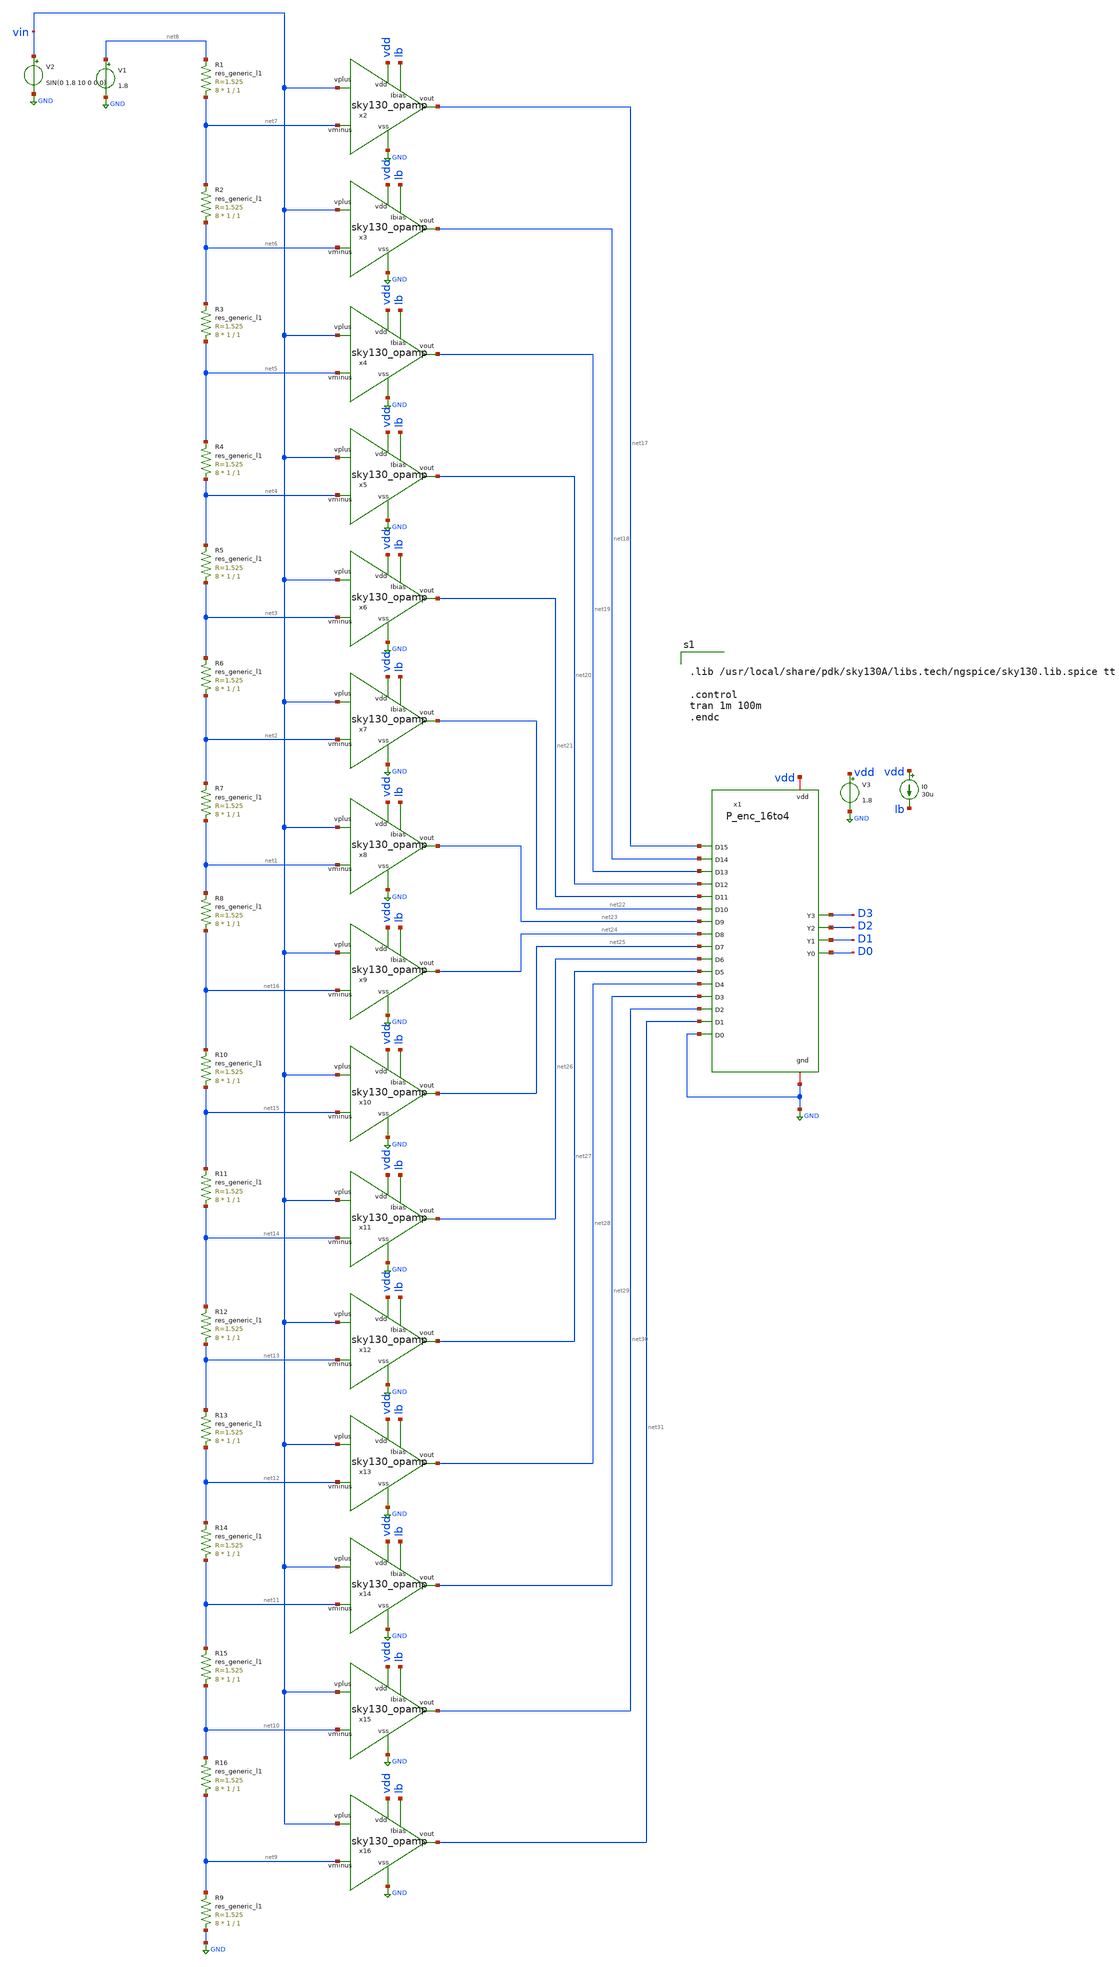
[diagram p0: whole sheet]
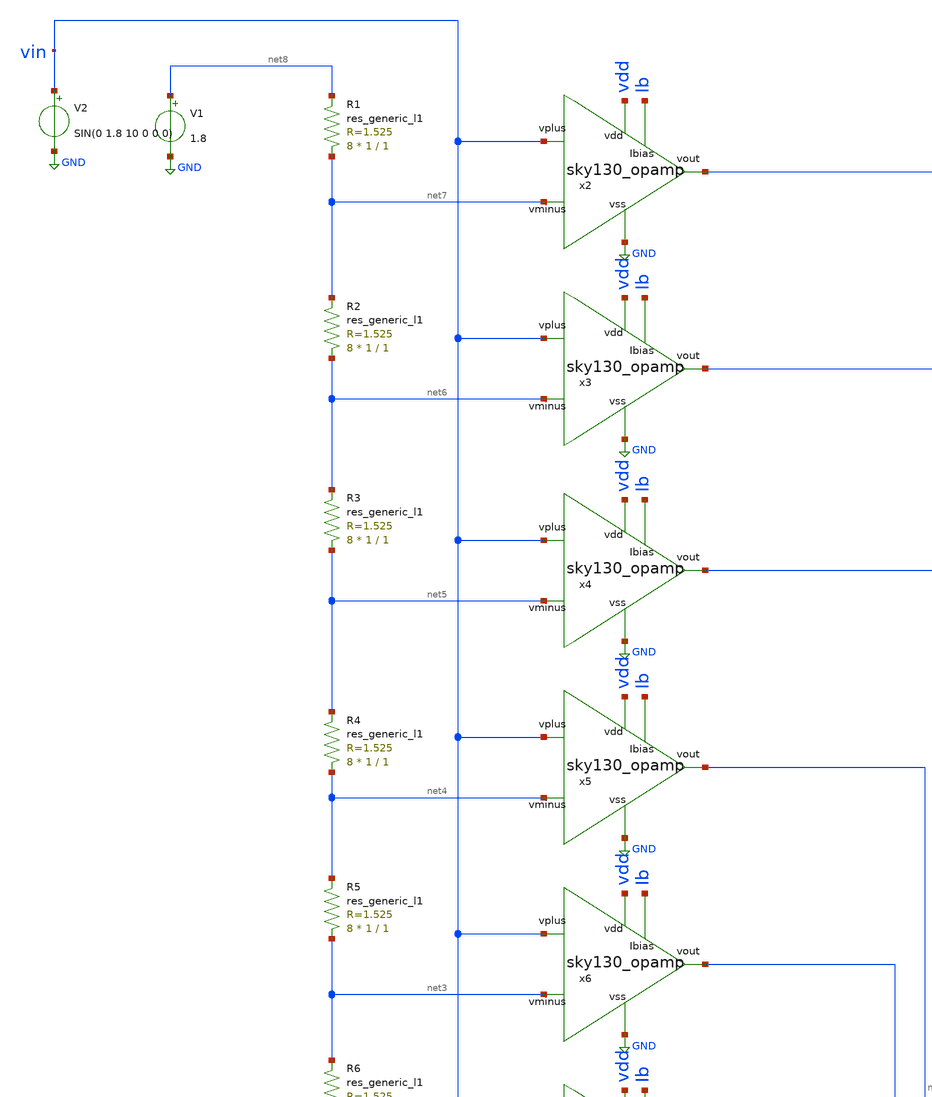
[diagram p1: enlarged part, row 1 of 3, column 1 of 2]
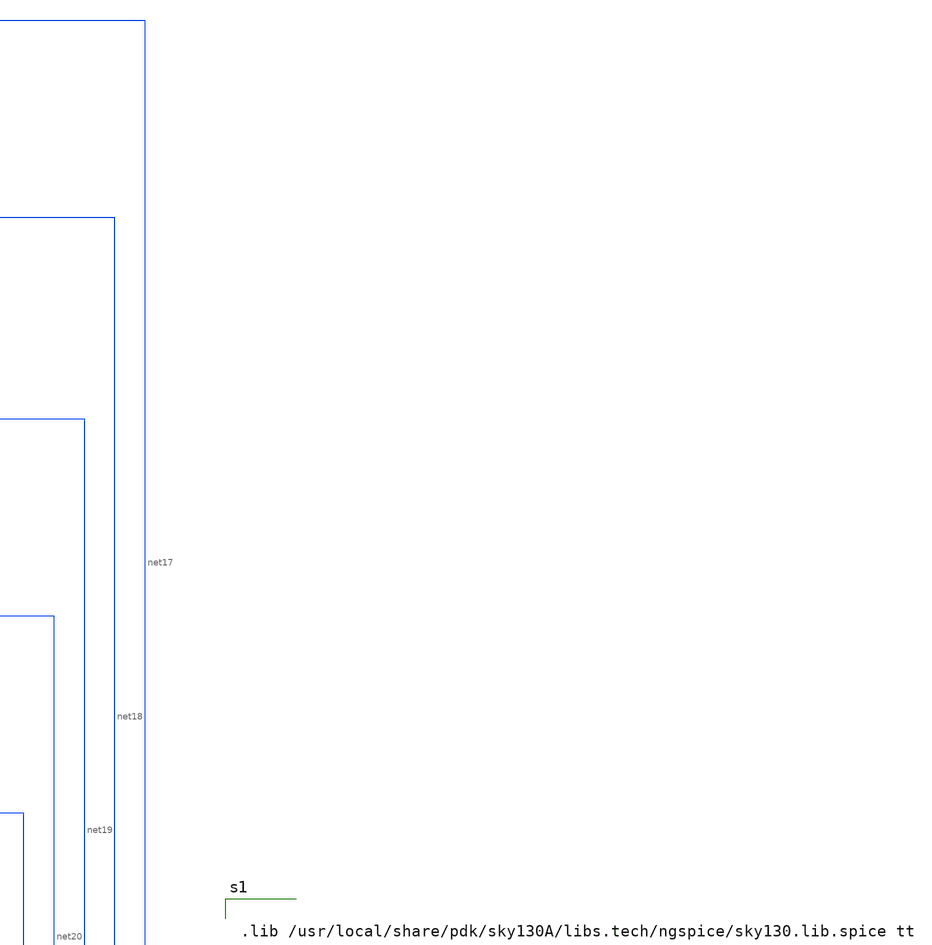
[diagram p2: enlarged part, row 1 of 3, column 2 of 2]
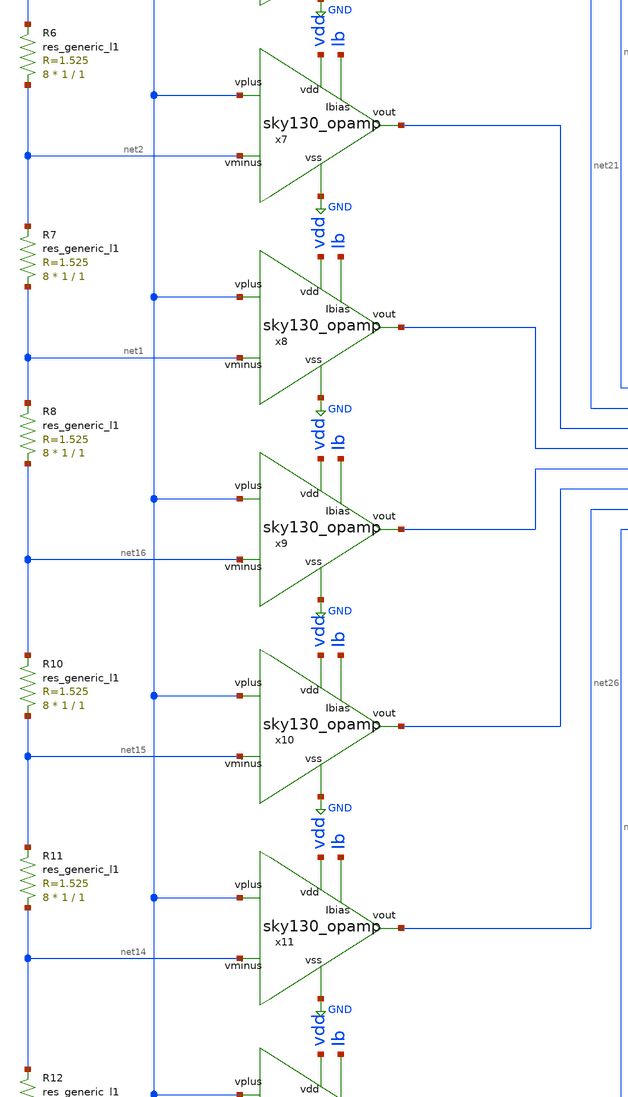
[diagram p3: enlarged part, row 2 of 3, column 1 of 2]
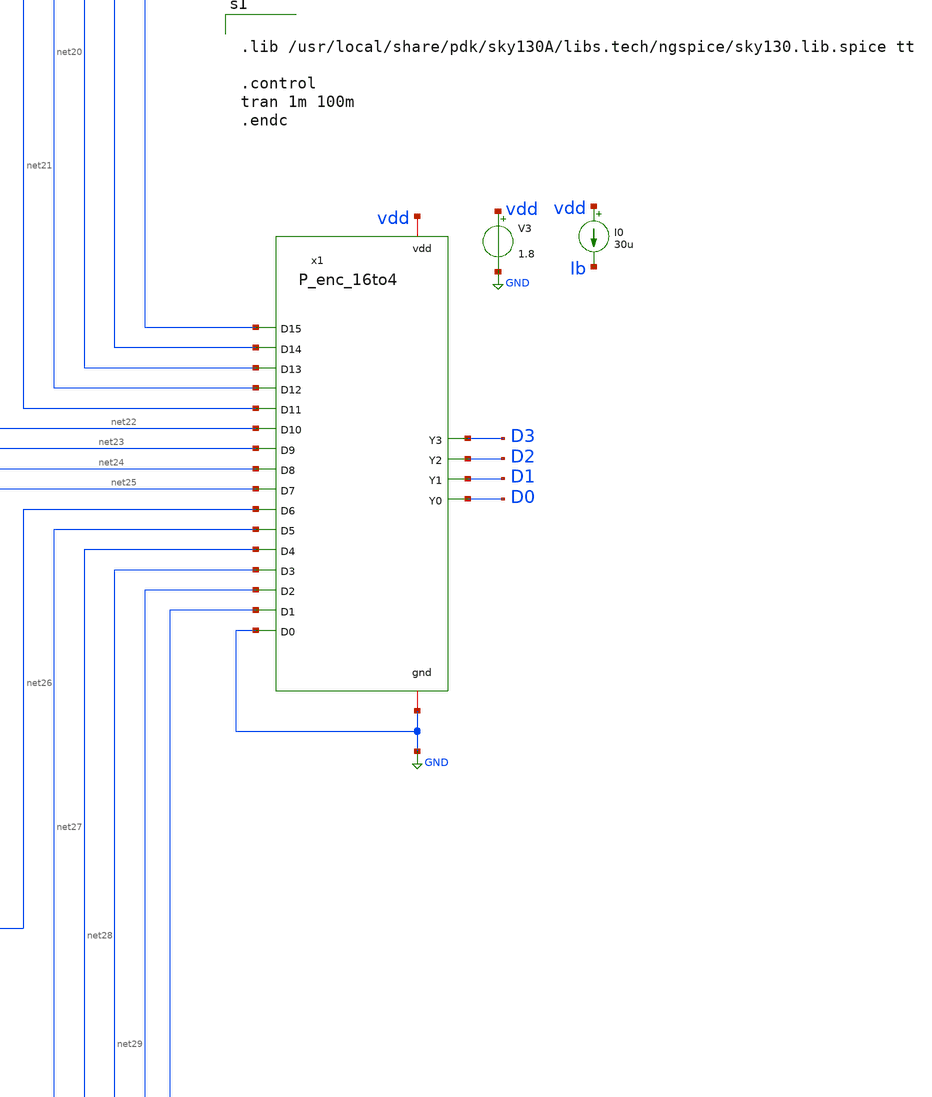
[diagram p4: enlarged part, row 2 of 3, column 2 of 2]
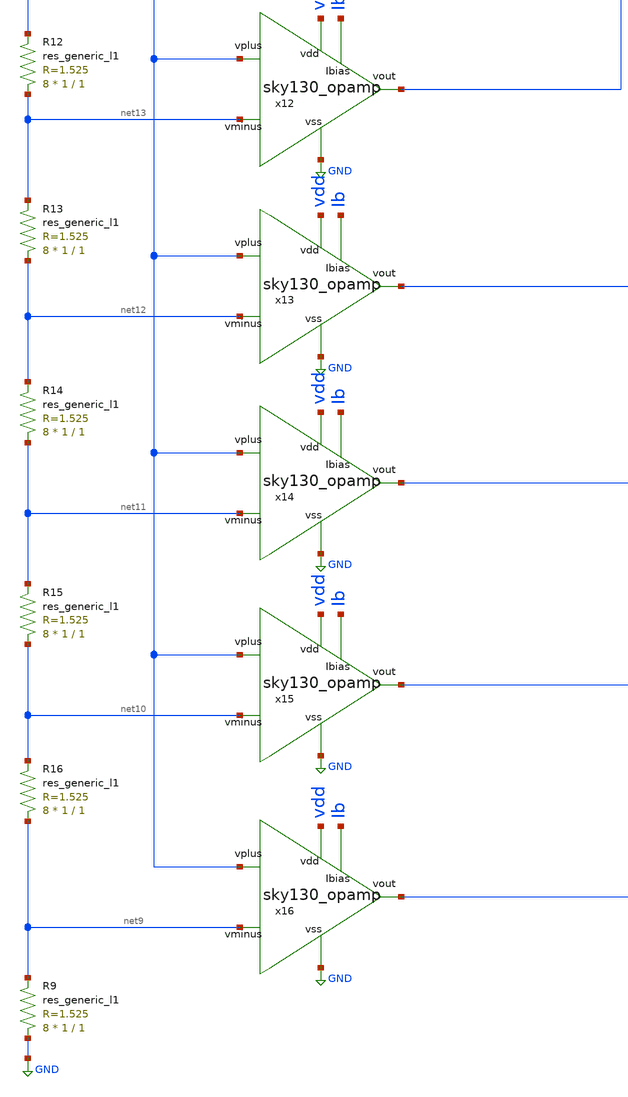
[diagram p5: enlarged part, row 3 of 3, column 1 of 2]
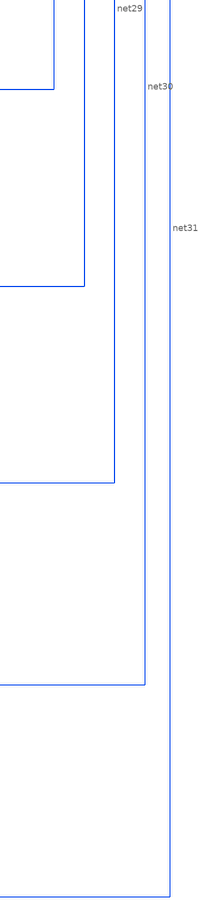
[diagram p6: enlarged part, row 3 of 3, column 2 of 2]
** sch_path: Analog to Digital Converter (Flash ADC)/Flash_adc_4bit.sch
**.subckt Flash_adc_4bit
x1 D3 vdd GND net17 net18 net19 D2 net20 net21 net22 D1 net23 net24 net25 net26 D0 net27 net28 net29
+ net30 net31 GND P_enc_16to4
x2 vdd net17 vin net7 Ib GND sky130_opamp
R1 net7 net8 sky130_fd_pr__res_generic_l1 W=1 L=1 m=8
R2 net6 net7 sky130_fd_pr__res_generic_l1 W=1 L=1 m=8
R3 net5 net6 sky130_fd_pr__res_generic_l1 W=1 L=1 m=8
R4 net4 net5 sky130_fd_pr__res_generic_l1 W=1 L=1 m=8
R5 net3 net4 sky130_fd_pr__res_generic_l1 W=1 L=1 m=8
R6 net2 net3 sky130_fd_pr__res_generic_l1 W=1 L=1 m=8
R7 net1 net2 sky130_fd_pr__res_generic_l1 W=1 L=1 m=8
R8 net16 net1 sky130_fd_pr__res_generic_l1 W=1 L=1 m=8
x3 vdd net18 vin net6 Ib GND sky130_opamp
x4 vdd net19 vin net5 Ib GND sky130_opamp
x5 vdd net20 vin net4 Ib GND sky130_opamp
x6 vdd net21 vin net3 Ib GND sky130_opamp
x7 vdd net22 vin net2 Ib GND sky130_opamp
x8 vdd net23 vin net1 Ib GND sky130_opamp
x9 vdd net24 vin net16 Ib GND sky130_opamp
x10 vdd net25 vin net15 Ib GND sky130_opamp
x11 vdd net26 vin net14 Ib GND sky130_opamp
x12 vdd net27 vin net13 Ib GND sky130_opamp
x13 vdd net28 vin net12 Ib GND sky130_opamp
x14 vdd net29 vin net11 Ib GND sky130_opamp
x15 vdd net30 vin net10 Ib GND sky130_opamp
R10 net15 net16 sky130_fd_pr__res_generic_l1 W=1 L=1 m=8
R11 net14 net15 sky130_fd_pr__res_generic_l1 W=1 L=1 m=8
R12 net13 net14 sky130_fd_pr__res_generic_l1 W=1 L=1 m=8
R13 net12 net13 sky130_fd_pr__res_generic_l1 W=1 L=1 m=8
R14 net11 net12 sky130_fd_pr__res_generic_l1 W=1 L=1 m=8
R15 net10 net11 sky130_fd_pr__res_generic_l1 W=1 L=1 m=8
R16 net9 net10 sky130_fd_pr__res_generic_l1 W=1 L=1 m=8
x16 vdd net31 vin net9 Ib GND sky130_opamp
R9 GND net9 sky130_fd_pr__res_generic_l1 W=1 L=1 m=8
V1 net8 GND 1.8
V2 vin GND SIN(0 1.8 10 0 0 0)
V3 vdd GND 1.8
I0 vdd Ib 30u
**** begin user architecture code


.lib /usr/local/share/pdk/sky130A/libs.tech/ngspice/sky130.lib.spice tt

.control
tran 1m 100m
.endc


**** end user architecture code
**.ends

* expanding   symbol:  /home/rachtih/ADC trials/P_enc/P_enc_16to4.sym # of pins=22
** sym_path: Primitives/Priority Encoder 16to4/Xschem Files/P_enc_16to4.sym
** sch_path: Primitives/Priority Encoder 16to4/Xschem Files/P_enc_16to4.sch
.subckt P_enc_16to4 Y3 vdd gnd D15 D14 D13 Y2 D12 D11 D10 Y1 D9 D8 D7 D6 Y0 D5 D4 D3 D2 D1 D0
*.iopin vdd
*.iopin gnd
*.ipin D0
*.ipin D1
*.ipin D2
*.ipin D3
*.ipin D4
*.ipin D5
*.ipin D6
*.ipin D7
*.ipin D8
*.ipin D9
*.ipin D10
*.ipin D11
*.ipin D12
*.ipin D13
*.ipin D14
*.ipin D15
*.opin Y0
*.opin Y1
*.opin Y2
*.opin Y3
x5 net5 vdd gnd net12 net4 net1 sky130_mux
x6 net7 vdd gnd net14 net6 net1 sky130_mux
x7 net9 vdd gnd net13 net8 net3 sky130_mux
x8 net11 vdd gnd net15 net10 net3 sky130_mux
x9 net3 vdd gnd Y2 net1 Y3 sky130_mux
x10 net13 vdd gnd Y1 net12 Y3 sky130_mux
x11 net15 vdd gnd Y0 net14 Y3 sky130_mux
x12 vdd net1 net2 Y3 gnd sky130_orgate
x3 vdd D11 D10 D9 D8 net7 net2 net5 gnd P_enc_4to2
x2 vdd D7 D6 D5 D4 net10 net3 net8 gnd P_enc_4to2
x1 vdd D3 D2 D1 D0 net11 net16 net9 gnd P_enc_4to2
x4 vdd D15 D14 D13 D12 net6 net1 net4 gnd P_enc_4to2
.ends


* expanding   symbol:  /home/rachtih/ADC trials/opamp/sky130_opamp.sym # of pins=6
** sym_path: Primitives/Operational Amplifier/Xschem Files/sky130_opamp.sym
** sch_path: Primitives/Operational Amplifier/Xschem Files/sky130_opamp.sch
.subckt sky130_opamp vdd vout vplus vminus Ibias vss
*.ipin Ibias
*.ipin vminus
*.ipin vplus
*.ipin vss
*.ipin vdd
*.opin vout
XM1 Ibias Ibias vss vss sky130_fd_pr__nfet_01v8 L=0.15 W=1 nf=1 ad='int((1 + 1)/2) * 1 / 1 * 0.29' as='int((1 + 2)/2) * 1 / 1 * 0.29'
+ pd='2*int((1 + 1)/2) * (1 / 1 + 0.29)' ps='2*int((1 + 2)/2) * (1 / 1 + 0.29)' nrd='0.29 / 1 ' nrs='0.29 / 1 '
+ sa=0 sb=0 sd=0 mult=1 m=1
XM2 net3 Ibias vss vss sky130_fd_pr__nfet_01v8 L=0.15 W=1 nf=1 ad='int((1 + 1)/2) * 1 / 1 * 0.29' as='int((1 + 2)/2) * 1 / 1 * 0.29'
+ pd='2*int((1 + 1)/2) * (1 / 1 + 0.29)' ps='2*int((1 + 2)/2) * (1 / 1 + 0.29)' nrd='0.29 / 1 ' nrs='0.29 / 1 '
+ sa=0 sb=0 sd=0 mult=1 m=1
XM3 net1 vminus net3 vss sky130_fd_pr__nfet_01v8 L=0.15 W=1 nf=1 ad='int((1 + 1)/2) * 1 / 1 * 0.29' as='int((1 + 2)/2) * 1 / 1 * 0.29'
+ pd='2*int((1 + 1)/2) * (1 / 1 + 0.29)' ps='2*int((1 + 2)/2) * (1 / 1 + 0.29)' nrd='0.29 / 1 ' nrs='0.29 / 1 '
+ sa=0 sb=0 sd=0 mult=1 m=1
XM4 net2 vplus net3 vss sky130_fd_pr__nfet_01v8 L=0.15 W=1 nf=1 ad='int((1 + 1)/2) * 1 / 1 * 0.29' as='int((1 + 2)/2) * 1 / 1 * 0.29'
+ pd='2*int((1 + 1)/2) * (1 / 1 + 0.29)' ps='2*int((1 + 2)/2) * (1 / 1 + 0.29)' nrd='0.29 / 1 ' nrs='0.29 / 1 '
+ sa=0 sb=0 sd=0 mult=1 m=1
XM5 vout Ibias vss vss sky130_fd_pr__nfet_01v8 L=0.15 W=1 nf=1 ad='int((1 + 1)/2) * 1 / 1 * 0.29' as='int((1 + 2)/2) * 1 / 1 * 0.29'
+ pd='2*int((1 + 1)/2) * (1 / 1 + 0.29)' ps='2*int((1 + 2)/2) * (1 / 1 + 0.29)' nrd='0.29 / 1 ' nrs='0.29 / 1 '
+ sa=0 sb=0 sd=0 mult=1 m=1
XM6 net2 net1 vdd vdd sky130_fd_pr__pfet_01v8 L=0.15 W=1 nf=1 ad='int((1 + 1)/2) * 1 / 1 * 0.29' as='int((1 + 2)/2) * 1 / 1 * 0.29'
+ pd='2*int((1 + 1)/2) * (1 / 1 + 0.29)' ps='2*int((1 + 2)/2) * (1 / 1 + 0.29)' nrd='0.29 / 1 ' nrs='0.29 / 1 '
+ sa=0 sb=0 sd=0 mult=1 m=1
XM7 net1 net1 vdd vdd sky130_fd_pr__pfet_01v8 L=0.15 W=1 nf=1 ad='int((1 + 1)/2) * 1 / 1 * 0.29' as='int((1 + 2)/2) * 1 / 1 * 0.29'
+ pd='2*int((1 + 1)/2) * (1 / 1 + 0.29)' ps='2*int((1 + 2)/2) * (1 / 1 + 0.29)' nrd='0.29 / 1 ' nrs='0.29 / 1 '
+ sa=0 sb=0 sd=0 mult=1 m=1
XM8 vout net2 vdd vdd sky130_fd_pr__pfet_01v8 L=0.15 W=1 nf=1 ad='int((1 + 1)/2) * 1 / 1 * 0.29' as='int((1 + 2)/2) * 1 / 1 * 0.29'
+ pd='2*int((1 + 1)/2) * (1 / 1 + 0.29)' ps='2*int((1 + 2)/2) * (1 / 1 + 0.29)' nrd='0.29 / 1 ' nrs='0.29 / 1 '
+ sa=0 sb=0 sd=0 mult=1 m=1
C1 net4 vout 2.7p m=1
R1 net2 net4 50 m=1
.ends


* expanding   symbol:  /home/rachtih/ADC trials/mux/sky130_mux.sym # of pins=6
** sym_path: Primitives/Multiplexer 2to1/Xschem Files/sky130_mux.sym
** sch_path: Primitives/Multiplexer 2to1/Xschem Files/sky130_mux.sch
.subckt sky130_mux in0 vdd gnd out in1 sel
*.iopin vdd
*.iopin gnd
*.ipin in0
*.ipin sel
*.ipin in1
*.opin out
XM1 net1 sel gnd gnd sky130_fd_pr__nfet_01v8 L=0.15 W=1 nf=1 ad='int((1 + 1)/2) * 1 / 1 * 0.29' as='int((1 + 2)/2) * 1 / 1 * 0.29'
+ pd='2*int((1 + 1)/2) * (1 / 1 + 0.29)' ps='2*int((1 + 2)/2) * (1 / 1 + 0.29)' nrd='0.29 / 1 ' nrs='0.29 / 1 '
+ sa=0 sb=0 sd=0 mult=1 m=1
XM2 net1 sel vdd vdd sky130_fd_pr__pfet_01v8 L=0.15 W=1 nf=1 ad='int((1 + 1)/2) * 1 / 1 * 0.29' as='int((1 + 2)/2) * 1 / 1 * 0.29'
+ pd='2*int((1 + 1)/2) * (1 / 1 + 0.29)' ps='2*int((1 + 2)/2) * (1 / 1 + 0.29)' nrd='0.29 / 1 ' nrs='0.29 / 1 '
+ sa=0 sb=0 sd=0 mult=1 m=1
XM3 in1 sel out gnd sky130_fd_pr__nfet_01v8 L=0.15 W=1 nf=1 ad='int((1 + 1)/2) * 1 / 1 * 0.29' as='int((1 + 2)/2) * 1 / 1 * 0.29'
+ pd='2*int((1 + 1)/2) * (1 / 1 + 0.29)' ps='2*int((1 + 2)/2) * (1 / 1 + 0.29)' nrd='0.29 / 1 ' nrs='0.29 / 1 '
+ sa=0 sb=0 sd=0 mult=1 m=1
XM4 in1 net1 out vdd sky130_fd_pr__pfet_01v8 L=0.15 W=1 nf=1 ad='int((1 + 1)/2) * 1 / 1 * 0.29' as='int((1 + 2)/2) * 1 / 1 * 0.29'
+ pd='2*int((1 + 1)/2) * (1 / 1 + 0.29)' ps='2*int((1 + 2)/2) * (1 / 1 + 0.29)' nrd='0.29 / 1 ' nrs='0.29 / 1 '
+ sa=0 sb=0 sd=0 mult=1 m=1
XM5 in0 net1 out gnd sky130_fd_pr__nfet_01v8 L=0.15 W=1 nf=1 ad='int((1 + 1)/2) * 1 / 1 * 0.29' as='int((1 + 2)/2) * 1 / 1 * 0.29'
+ pd='2*int((1 + 1)/2) * (1 / 1 + 0.29)' ps='2*int((1 + 2)/2) * (1 / 1 + 0.29)' nrd='0.29 / 1 ' nrs='0.29 / 1 '
+ sa=0 sb=0 sd=0 mult=1 m=1
XM6 in0 sel out vdd sky130_fd_pr__pfet_01v8 L=0.15 W=1 nf=1 ad='int((1 + 1)/2) * 1 / 1 * 0.29' as='int((1 + 2)/2) * 1 / 1 * 0.29'
+ pd='2*int((1 + 1)/2) * (1 / 1 + 0.29)' ps='2*int((1 + 2)/2) * (1 / 1 + 0.29)' nrd='0.29 / 1 ' nrs='0.29 / 1 '
+ sa=0 sb=0 sd=0 mult=1 m=1
.ends


* expanding   symbol:  /home/rachtih/ADC trials/or_gate/sky130_orgate.sym # of pins=5
** sym_path: Primitives/OR Gate/Xschem Files/sky130_orgate.sym
** sch_path: Primitives/OR Gate/Xschem Files/sky130_orgate.sch
.subckt sky130_orgate vdd A B Y gnd
*.ipin A
*.ipin B
*.iopin gnd
*.iopin vdd
*.opin Y
XM1 net1 B gnd gnd sky130_fd_pr__nfet_01v8 L=0.15 W=1 nf=1 ad='int((1 + 1)/2) * 1 / 1 * 0.29' as='int((1 + 2)/2) * 1 / 1 * 0.29'
+ pd='2*int((1 + 1)/2) * (1 / 1 + 0.29)' ps='2*int((1 + 2)/2) * (1 / 1 + 0.29)' nrd='0.29 / 1 ' nrs='0.29 / 1 '
+ sa=0 sb=0 sd=0 mult=1 m=1
XM2 net2 A vdd vdd sky130_fd_pr__pfet_01v8 L=0.15 W=1 nf=1 ad='int((1 + 1)/2) * 1 / 1 * 0.29' as='int((1 + 2)/2) * 1 / 1 * 0.29'
+ pd='2*int((1 + 1)/2) * (1 / 1 + 0.29)' ps='2*int((1 + 2)/2) * (1 / 1 + 0.29)' nrd='0.29 / 1 ' nrs='0.29 / 1 '
+ sa=0 sb=0 sd=0 mult=1 m=1
XM3 net1 A gnd gnd sky130_fd_pr__nfet_01v8 L=0.15 W=1 nf=1 ad='int((1 + 1)/2) * 1 / 1 * 0.29' as='int((1 + 2)/2) * 1 / 1 * 0.29'
+ pd='2*int((1 + 1)/2) * (1 / 1 + 0.29)' ps='2*int((1 + 2)/2) * (1 / 1 + 0.29)' nrd='0.29 / 1 ' nrs='0.29 / 1 '
+ sa=0 sb=0 sd=0 mult=1 m=1
XM4 net1 B net2 vdd sky130_fd_pr__pfet_01v8 L=0.15 W=1 nf=1 ad='int((1 + 1)/2) * 1 / 1 * 0.29' as='int((1 + 2)/2) * 1 / 1 * 0.29'
+ pd='2*int((1 + 1)/2) * (1 / 1 + 0.29)' ps='2*int((1 + 2)/2) * (1 / 1 + 0.29)' nrd='0.29 / 1 ' nrs='0.29 / 1 '
+ sa=0 sb=0 sd=0 mult=1 m=1
XM5 Y net1 vdd vdd sky130_fd_pr__pfet_01v8 L=0.15 W=1 nf=1 ad='int((1 + 1)/2) * 1 / 1 * 0.29' as='int((1 + 2)/2) * 1 / 1 * 0.29'
+ pd='2*int((1 + 1)/2) * (1 / 1 + 0.29)' ps='2*int((1 + 2)/2) * (1 / 1 + 0.29)' nrd='0.29 / 1 ' nrs='0.29 / 1 '
+ sa=0 sb=0 sd=0 mult=1 m=1
XM6 Y net1 gnd gnd sky130_fd_pr__nfet_01v8 L=0.15 W=1 nf=1 ad='int((1 + 1)/2) * 1 / 1 * 0.29' as='int((1 + 2)/2) * 1 / 1 * 0.29'
+ pd='2*int((1 + 1)/2) * (1 / 1 + 0.29)' ps='2*int((1 + 2)/2) * (1 / 1 + 0.29)' nrd='0.29 / 1 ' nrs='0.29 / 1 '
+ sa=0 sb=0 sd=0 mult=1 m=1
.ends


* expanding   symbol:  /home/rachtih/ADC trials/P_enc/P_enc_4to2.sym # of pins=9
** sym_path: Primitives/Priority Encoder 4to2/Xschem Files/P_enc_4to2.sym
** sch_path: Primitives/Priority Encoder 4to2/Xschem Files/P_enc_4to2.sch
.subckt P_enc_4to2 vdd D3 D2 D1 D0 out0 valid out1 gnd
*.opin valid
*.iopin vdd
*.iopin gnd
*.opin out1
*.opin out0
*.ipin D3
*.ipin D2
*.ipin D1
*.ipin D0
XM5 net7 D3 vdd vdd sky130_fd_pr__pfet_01v8 L=0.15 W=1 nf=1 ad='int((1 + 1)/2) * 1 / 1 * 0.29' as='int((1 + 2)/2) * 1 / 1 * 0.29'
+ pd='2*int((1 + 1)/2) * (1 / 1 + 0.29)' ps='2*int((1 + 2)/2) * (1 / 1 + 0.29)' nrd='0.29 / 1 ' nrs='0.29 / 1 '
+ sa=0 sb=0 sd=0 mult=1 m=1
XM6 net8 D2 net7 vdd sky130_fd_pr__pfet_01v8 L=0.15 W=1 nf=1 ad='int((1 + 1)/2) * 1 / 1 * 0.29' as='int((1 + 2)/2) * 1 / 1 * 0.29'
+ pd='2*int((1 + 1)/2) * (1 / 1 + 0.29)' ps='2*int((1 + 2)/2) * (1 / 1 + 0.29)' nrd='0.29 / 1 ' nrs='0.29 / 1 '
+ sa=0 sb=0 sd=0 mult=1 m=1
XM7 net9 D1 net8 vdd sky130_fd_pr__pfet_01v8 L=0.15 W=1 nf=1 ad='int((1 + 1)/2) * 1 / 1 * 0.29' as='int((1 + 2)/2) * 1 / 1 * 0.29'
+ pd='2*int((1 + 1)/2) * (1 / 1 + 0.29)' ps='2*int((1 + 2)/2) * (1 / 1 + 0.29)' nrd='0.29 / 1 ' nrs='0.29 / 1 '
+ sa=0 sb=0 sd=0 mult=1 m=1
XM8 net1 D0 net9 vdd sky130_fd_pr__pfet_01v8 L=0.15 W=1 nf=1 ad='int((1 + 1)/2) * 1 / 1 * 0.29' as='int((1 + 2)/2) * 1 / 1 * 0.29'
+ pd='2*int((1 + 1)/2) * (1 / 1 + 0.29)' ps='2*int((1 + 2)/2) * (1 / 1 + 0.29)' nrd='0.29 / 1 ' nrs='0.29 / 1 '
+ sa=0 sb=0 sd=0 mult=1 m=1
XM9 net1 D0 gnd gnd sky130_fd_pr__nfet_01v8 L=0.15 W=1 nf=1 ad='int((1 + 1)/2) * 1 / 1 * 0.29' as='int((1 + 2)/2) * 1 / 1 * 0.29'
+ pd='2*int((1 + 1)/2) * (1 / 1 + 0.29)' ps='2*int((1 + 2)/2) * (1 / 1 + 0.29)' nrd='0.29 / 1 ' nrs='0.29 / 1 '
+ sa=0 sb=0 sd=0 mult=1 m=1
XM10 net1 D1 gnd gnd sky130_fd_pr__nfet_01v8 L=0.15 W=1 nf=1 ad='int((1 + 1)/2) * 1 / 1 * 0.29' as='int((1 + 2)/2) * 1 / 1 * 0.29'
+ pd='2*int((1 + 1)/2) * (1 / 1 + 0.29)' ps='2*int((1 + 2)/2) * (1 / 1 + 0.29)' nrd='0.29 / 1 ' nrs='0.29 / 1 '
+ sa=0 sb=0 sd=0 mult=1 m=1
XM11 net1 D2 gnd gnd sky130_fd_pr__nfet_01v8 L=0.15 W=1 nf=1 ad='int((1 + 1)/2) * 1 / 1 * 0.29' as='int((1 + 2)/2) * 1 / 1 * 0.29'
+ pd='2*int((1 + 1)/2) * (1 / 1 + 0.29)' ps='2*int((1 + 2)/2) * (1 / 1 + 0.29)' nrd='0.29 / 1 ' nrs='0.29 / 1 '
+ sa=0 sb=0 sd=0 mult=1 m=1
XM12 net1 D3 gnd gnd sky130_fd_pr__nfet_01v8 L=0.15 W=1 nf=1 ad='int((1 + 1)/2) * 1 / 1 * 0.29' as='int((1 + 2)/2) * 1 / 1 * 0.29'
+ pd='2*int((1 + 1)/2) * (1 / 1 + 0.29)' ps='2*int((1 + 2)/2) * (1 / 1 + 0.29)' nrd='0.29 / 1 ' nrs='0.29 / 1 '
+ sa=0 sb=0 sd=0 mult=1 m=1
XM13 valid net1 gnd gnd sky130_fd_pr__nfet_01v8 L=0.15 W=1 nf=1 ad='int((1 + 1)/2) * 1 / 1 * 0.29' as='int((1 + 2)/2) * 1 / 1 * 0.29'
+ pd='2*int((1 + 1)/2) * (1 / 1 + 0.29)' ps='2*int((1 + 2)/2) * (1 / 1 + 0.29)' nrd='0.29 / 1 ' nrs='0.29 / 1 '
+ sa=0 sb=0 sd=0 mult=1 m=1
XM14 valid net1 vdd vdd sky130_fd_pr__pfet_01v8 L=0.15 W=1 nf=1 ad='int((1 + 1)/2) * 1 / 1 * 0.29' as='int((1 + 2)/2) * 1 / 1 * 0.29'
+ pd='2*int((1 + 1)/2) * (1 / 1 + 0.29)' ps='2*int((1 + 2)/2) * (1 / 1 + 0.29)' nrd='0.29 / 1 ' nrs='0.29 / 1 '
+ sa=0 sb=0 sd=0 mult=1 m=1
XM17 net2 D2 gnd gnd sky130_fd_pr__nfet_01v8 L=0.15 W=1 nf=1 ad='int((1 + 1)/2) * 1 / 1 * 0.29' as='int((1 + 2)/2) * 1 / 1 * 0.29'
+ pd='2*int((1 + 1)/2) * (1 / 1 + 0.29)' ps='2*int((1 + 2)/2) * (1 / 1 + 0.29)' nrd='0.29 / 1 ' nrs='0.29 / 1 '
+ sa=0 sb=0 sd=0 mult=1 m=1
XM18 net2 D2 vdd vdd sky130_fd_pr__pfet_01v8 L=0.15 W=1 nf=1 ad='int((1 + 1)/2) * 1 / 1 * 0.29' as='int((1 + 2)/2) * 1 / 1 * 0.29'
+ pd='2*int((1 + 1)/2) * (1 / 1 + 0.29)' ps='2*int((1 + 2)/2) * (1 / 1 + 0.29)' nrd='0.29 / 1 ' nrs='0.29 / 1 '
+ sa=0 sb=0 sd=0 mult=1 m=1
XM19 net4 D3 vdd vdd sky130_fd_pr__pfet_01v8 L=0.15 W=1 nf=1 ad='int((1 + 1)/2) * 1 / 1 * 0.29' as='int((1 + 2)/2) * 1 / 1 * 0.29'
+ pd='2*int((1 + 1)/2) * (1 / 1 + 0.29)' ps='2*int((1 + 2)/2) * (1 / 1 + 0.29)' nrd='0.29 / 1 ' nrs='0.29 / 1 '
+ sa=0 sb=0 sd=0 mult=1 m=1
XM20 net3 net2 net4 vdd sky130_fd_pr__pfet_01v8 L=0.15 W=1 nf=1 ad='int((1 + 1)/2) * 1 / 1 * 0.29' as='int((1 + 2)/2) * 1 / 1 * 0.29'
+ pd='2*int((1 + 1)/2) * (1 / 1 + 0.29)' ps='2*int((1 + 2)/2) * (1 / 1 + 0.29)' nrd='0.29 / 1 ' nrs='0.29 / 1 '
+ sa=0 sb=0 sd=0 mult=1 m=1
XM21 net3 D1 net4 vdd sky130_fd_pr__pfet_01v8 L=0.15 W=1 nf=1 ad='int((1 + 1)/2) * 1 / 1 * 0.29' as='int((1 + 2)/2) * 1 / 1 * 0.29'
+ pd='2*int((1 + 1)/2) * (1 / 1 + 0.29)' ps='2*int((1 + 2)/2) * (1 / 1 + 0.29)' nrd='0.29 / 1 ' nrs='0.29 / 1 '
+ sa=0 sb=0 sd=0 mult=1 m=1
XM22 net3 D3 gnd gnd sky130_fd_pr__nfet_01v8 L=0.15 W=1 nf=1 ad='int((1 + 1)/2) * 1 / 1 * 0.29' as='int((1 + 2)/2) * 1 / 1 * 0.29'
+ pd='2*int((1 + 1)/2) * (1 / 1 + 0.29)' ps='2*int((1 + 2)/2) * (1 / 1 + 0.29)' nrd='0.29 / 1 ' nrs='0.29 / 1 '
+ sa=0 sb=0 sd=0 mult=1 m=1
XM23 net3 net2 net10 gnd sky130_fd_pr__nfet_01v8 L=0.15 W=1 nf=1 ad='int((1 + 1)/2) * 1 / 1 * 0.29' as='int((1 + 2)/2) * 1 / 1 * 0.29'
+ pd='2*int((1 + 1)/2) * (1 / 1 + 0.29)' ps='2*int((1 + 2)/2) * (1 / 1 + 0.29)' nrd='0.29 / 1 ' nrs='0.29 / 1 '
+ sa=0 sb=0 sd=0 mult=1 m=1
XM24 net10 D1 gnd gnd sky130_fd_pr__nfet_01v8 L=0.15 W=1 nf=1 ad='int((1 + 1)/2) * 1 / 1 * 0.29' as='int((1 + 2)/2) * 1 / 1 * 0.29'
+ pd='2*int((1 + 1)/2) * (1 / 1 + 0.29)' ps='2*int((1 + 2)/2) * (1 / 1 + 0.29)' nrd='0.29 / 1 ' nrs='0.29 / 1 '
+ sa=0 sb=0 sd=0 mult=1 m=1
XM25 out0 net3 vdd vdd sky130_fd_pr__pfet_01v8 L=0.15 W=1 nf=1 ad='int((1 + 1)/2) * 1 / 1 * 0.29' as='int((1 + 2)/2) * 1 / 1 * 0.29'
+ pd='2*int((1 + 1)/2) * (1 / 1 + 0.29)' ps='2*int((1 + 2)/2) * (1 / 1 + 0.29)' nrd='0.29 / 1 ' nrs='0.29 / 1 '
+ sa=0 sb=0 sd=0 mult=1 m=1
XM26 out0 net3 gnd gnd sky130_fd_pr__nfet_01v8 L=0.15 W=1 nf=1 ad='int((1 + 1)/2) * 1 / 1 * 0.29' as='int((1 + 2)/2) * 1 / 1 * 0.29'
+ pd='2*int((1 + 1)/2) * (1 / 1 + 0.29)' ps='2*int((1 + 2)/2) * (1 / 1 + 0.29)' nrd='0.29 / 1 ' nrs='0.29 / 1 '
+ sa=0 sb=0 sd=0 mult=1 m=1
XM1 net5 D3 gnd gnd sky130_fd_pr__nfet_01v8 L=0.15 W=1 nf=1 ad='int((1 + 1)/2) * 1 / 1 * 0.29' as='int((1 + 2)/2) * 1 / 1 * 0.29'
+ pd='2*int((1 + 1)/2) * (1 / 1 + 0.29)' ps='2*int((1 + 2)/2) * (1 / 1 + 0.29)' nrd='0.29 / 1 ' nrs='0.29 / 1 '
+ sa=0 sb=0 sd=0 mult=1 m=1
XM2 net5 D2 net6 vdd sky130_fd_pr__pfet_01v8 L=0.15 W=1 nf=1 ad='int((1 + 1)/2) * 1 / 1 * 0.29' as='int((1 + 2)/2) * 1 / 1 * 0.29'
+ pd='2*int((1 + 1)/2) * (1 / 1 + 0.29)' ps='2*int((1 + 2)/2) * (1 / 1 + 0.29)' nrd='0.29 / 1 ' nrs='0.29 / 1 '
+ sa=0 sb=0 sd=0 mult=1 m=1
XM3 net6 D3 vdd vdd sky130_fd_pr__pfet_01v8 L=0.15 W=1 nf=1 ad='int((1 + 1)/2) * 1 / 1 * 0.29' as='int((1 + 2)/2) * 1 / 1 * 0.29'
+ pd='2*int((1 + 1)/2) * (1 / 1 + 0.29)' ps='2*int((1 + 2)/2) * (1 / 1 + 0.29)' nrd='0.29 / 1 ' nrs='0.29 / 1 '
+ sa=0 sb=0 sd=0 mult=1 m=1
XM4 net5 D2 gnd gnd sky130_fd_pr__nfet_01v8 L=0.15 W=1 nf=1 ad='int((1 + 1)/2) * 1 / 1 * 0.29' as='int((1 + 2)/2) * 1 / 1 * 0.29'
+ pd='2*int((1 + 1)/2) * (1 / 1 + 0.29)' ps='2*int((1 + 2)/2) * (1 / 1 + 0.29)' nrd='0.29 / 1 ' nrs='0.29 / 1 '
+ sa=0 sb=0 sd=0 mult=1 m=1
XM15 out1 net5 gnd gnd sky130_fd_pr__nfet_01v8 L=0.15 W=1 nf=1 ad='int((1 + 1)/2) * 1 / 1 * 0.29' as='int((1 + 2)/2) * 1 / 1 * 0.29'
+ pd='2*int((1 + 1)/2) * (1 / 1 + 0.29)' ps='2*int((1 + 2)/2) * (1 / 1 + 0.29)' nrd='0.29 / 1 ' nrs='0.29 / 1 '
+ sa=0 sb=0 sd=0 mult=1 m=1
XM16 out1 net5 vdd vdd sky130_fd_pr__pfet_01v8 L=0.15 W=1 nf=1 ad='int((1 + 1)/2) * 1 / 1 * 0.29' as='int((1 + 2)/2) * 1 / 1 * 0.29'
+ pd='2*int((1 + 1)/2) * (1 / 1 + 0.29)' ps='2*int((1 + 2)/2) * (1 / 1 + 0.29)' nrd='0.29 / 1 ' nrs='0.29 / 1 '
+ sa=0 sb=0 sd=0 mult=1 m=1
.ends

.GLOBAL GND
.end
